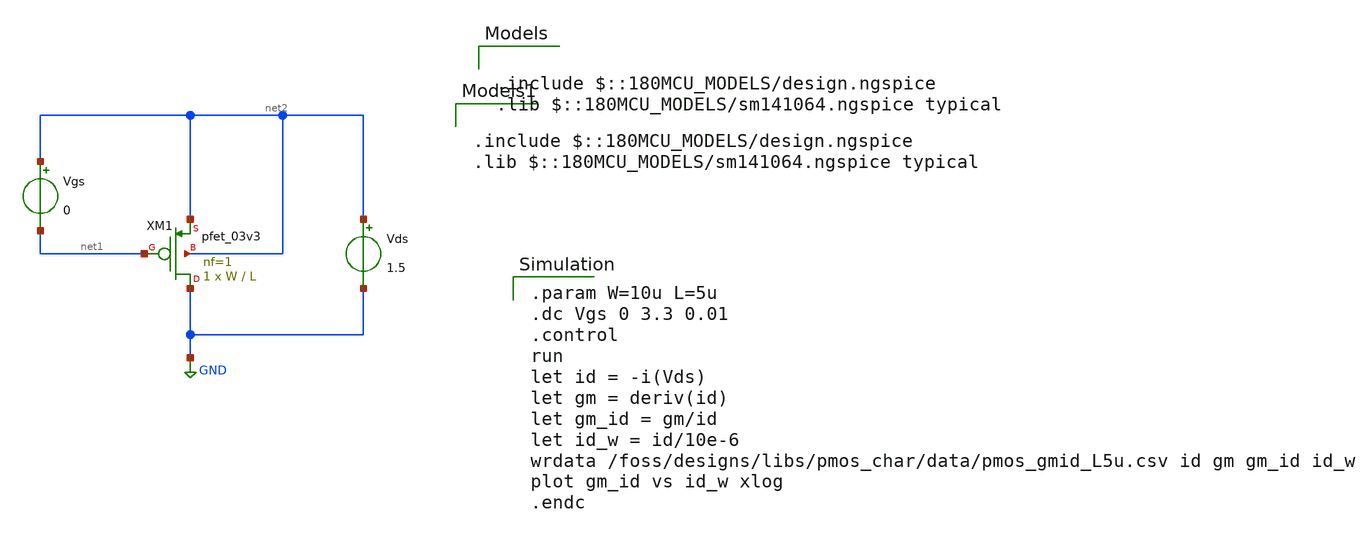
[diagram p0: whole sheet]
** sch_path: designs/libs/pmos_char/pmos_characterization.sch
**.subckt pmos_characterization
XM1 GND net1 net2 net2 pfet_03v3 L=L W=W nf=1 ad='int((nf+1)/2) * W/nf * 0.18u' as='int((nf+2)/2) * W/nf * 0.18u'
+ pd='2*int((nf+1)/2) * (W/nf + 0.18u)' ps='2*int((nf+2)/2) * (W/nf + 0.18u)' nrd='0.18u / W' nrs='0.18u / W'
+ sa=0 sb=0 sd=0 m=1
Vds net2 GND 1.5
Vgs net2 net1 0
**** begin user architecture code

.include $::180MCU_MODELS/design.ngspice
.lib $::180MCU_MODELS/sm141064.ngspice typical


.param W=10u L=5u
.dc Vgs 0 3.3 0.01
.control
run
let id = -i(Vds)
let gm = deriv(id)
let gm_id = gm/id
let id_w = id/10e-6
wrdata /foss/designs/libs/pmos_char/data/pmos_gmid_L5u.csv id gm gm_id id_w
plot gm_id vs id_w xlog
.endc


.include $::180MCU_MODELS/design.ngspice
.lib $::180MCU_MODELS/sm141064.ngspice typical

**** end user architecture code
**.ends
.GLOBAL GND
.end
